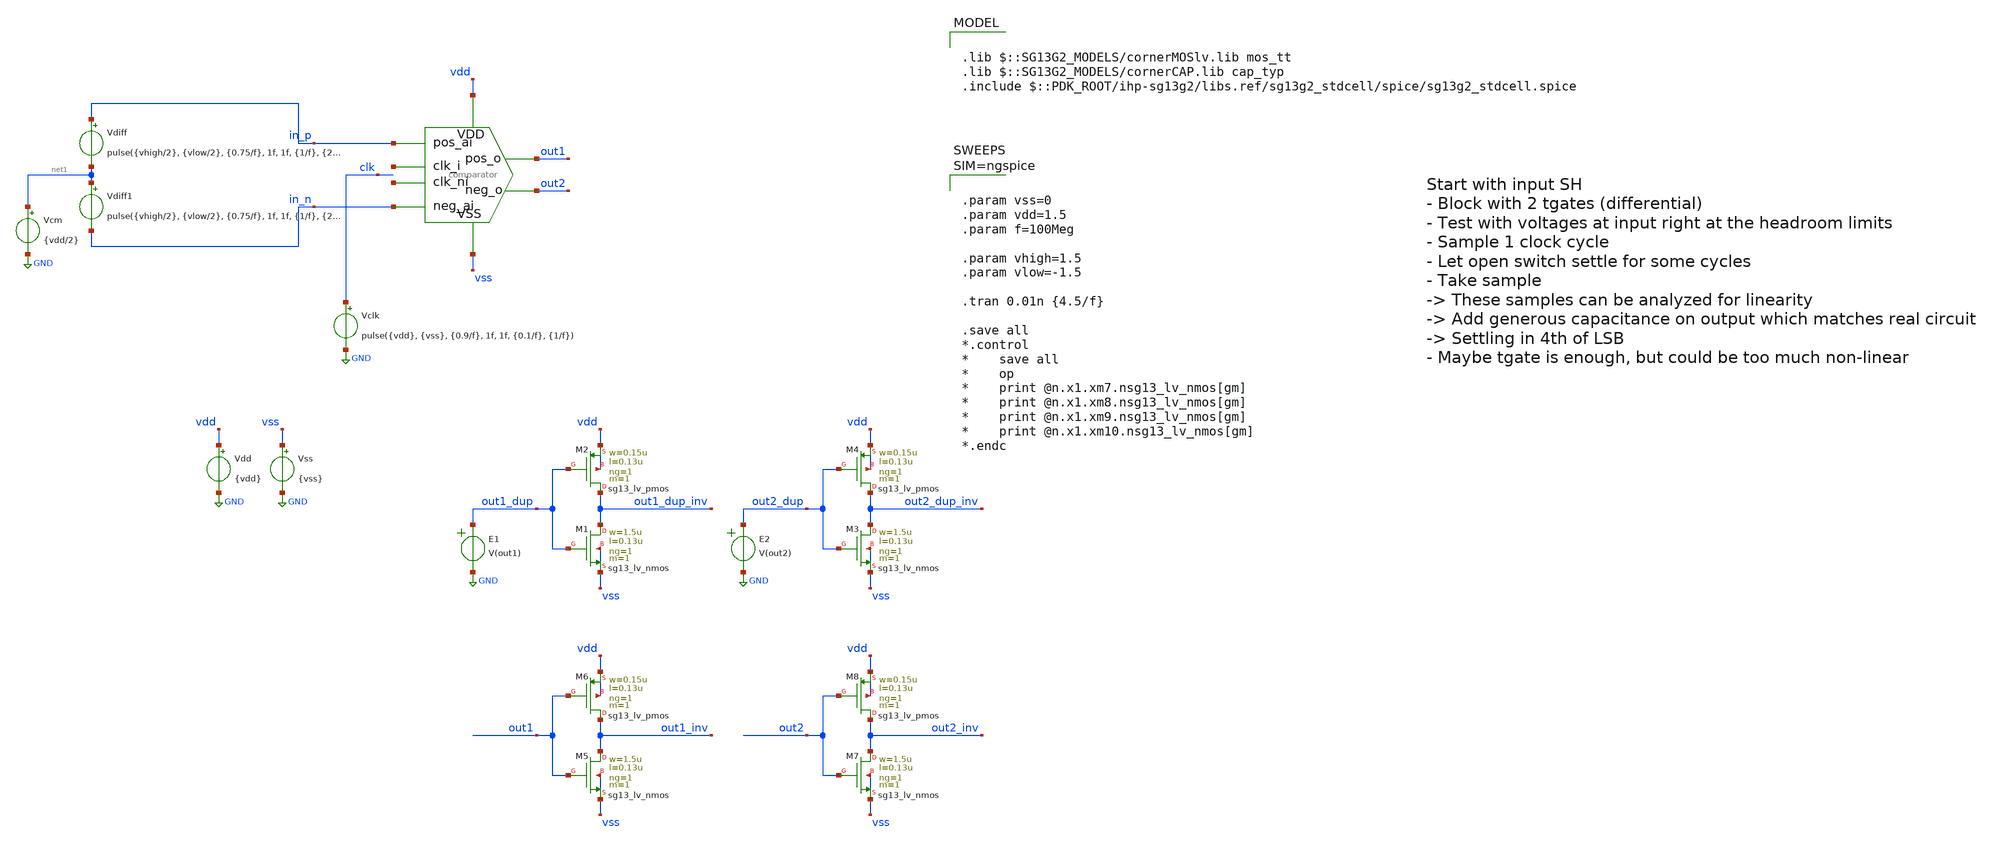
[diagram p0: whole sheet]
** sch_path: designs/comparator/comparator_tb.sch
**.subckt comparator_tb
x1 net2 in_p in_n out2 out1 vss vdd net3 comparator
Vdd vdd GND {vdd}
Vss vss GND {vss}
Vclk clk GND pulse({vdd}, {vss}, {0.9/f}, 1f, 1f, {0.1/f}, {1/f})
Vdiff in_p net1 pulse({vhigh/2}, {vlow/2}, {0.75/f}, 1f, 1f, {1/f}, {2/f})
Vcm net1 GND {vdd/2}
E1 out1_dup GND VOL=' V(out1) '
E2 out2_dup GND VOL=' V(out2) '
XM5 out1_inv out1 vss vss sg13_lv_nmos w=1.5u l=0.13u ng=1 m=1 mm_ok=1
XM6 out1_inv out1 vdd vdd sg13_lv_pmos w=0.15u l=0.13u ng=1 m=1 mm_ok=1
XM7 out2_inv out2 vss vss sg13_lv_nmos w=1.5u l=0.13u ng=1 m=1 mm_ok=1
XM8 out2_inv out2 vdd vdd sg13_lv_pmos w=0.15u l=0.13u ng=1 m=1 mm_ok=1
XM1 out1_dup_inv out1_dup vss vss sg13_lv_nmos w=1.5u l=0.13u ng=1 m=1 mm_ok=1
XM2 out1_dup_inv out1_dup vdd vdd sg13_lv_pmos w=0.15u l=0.13u ng=1 m=1 mm_ok=1
XM3 out2_dup_inv out2_dup vss vss sg13_lv_nmos w=1.5u l=0.13u ng=1 m=1 mm_ok=1
XM4 out2_dup_inv out2_dup vdd vdd sg13_lv_pmos w=0.15u l=0.13u ng=1 m=1 mm_ok=1
Vdiff1 net1 in_n pulse({vhigh/2}, {vlow/2}, {0.75/f}, 1f, 1f, {1/f}, {2/f})
**** begin user architecture code

.lib $::SG13G2_MODELS/cornerMOSlv.lib mos_tt
.lib $::SG13G2_MODELS/cornerCAP.lib cap_typ
.include $::PDK_ROOT/ihp-sg13g2/libs.ref/sg13g2_stdcell/spice/sg13g2_stdcell.spice




.param vss=0
.param vdd=1.5
.param f=100Meg

.param vhigh=1.5
.param vlow=-1.5

.tran 0.01n {4.5/f}

.save all
*.control
*	save all
*	op
*	print @n.x1.xm7.nsg13_lv_nmos[gm]
*	print @n.x1.xm8.nsg13_lv_nmos[gm]
*	print @n.x1.xm9.nsg13_lv_nmos[gm]
*	print @n.x1.xm10.nsg13_lv_nmos[gm]
*.endc



**** end user architecture code
**.ends

* expanding   symbol:  comparator.sym # of pins=8
** sym_path: designs/comparator_dt/comparator.sym
** sch_path: designs/comparator_dt/comparator.sch
.subckt comparator clk_i pos_ai neg_ai neg_o pos_o VSS VDD clk_ni
*.ipin pos_ai
*.ipin neg_ai
*.ipin VSS
*.ipin VDD
*.opin neg_o
*.opin pos_o
*.ipin clk_i
*.ipin clk_ni
XM12 neg_buf clk_i VDD VDD sg13_lv_pmos w=1.0u l=0.13u ng=1 m=1 mm_ok=1
XM13 pos_buf clk_i VDD VDD sg13_lv_pmos w=1.0u l=0.13u ng=1 m=1 mm_ok=1
XM14 net1 pos_ai neg_buf VSS sg13_lv_nmos w=1.0u l=0.13u ng=1 m=1 mm_ok=1
XM15 net1 neg_ai pos_buf VSS sg13_lv_nmos w=1.0u l=0.13u ng=1 m=1 mm_ok=1
XM16 VSS clk_i net1 VSS sg13_lv_nmos w=1.0u l=0.13u ng=1 m=1 mm_ok=1
XM17 net2 clk_ni VDD VDD sg13_lv_pmos w=2.0u l=0.13u ng=2 m=1 mm_ok=1
XM18 pos_o neg_o net2 VDD sg13_lv_pmos w=2.0u l=0.13u ng=2 m=1 mm_ok=1
XM19 neg_o pos_o net2 VDD sg13_lv_pmos w=2.0u l=0.13u ng=2 m=1 mm_ok=1
XM20 VSS neg_buf pos_o VSS sg13_lv_nmos w=1.0u l=0.13u ng=1 m=1 mm_ok=1
XM21 VSS neg_o pos_o VSS sg13_lv_nmos w=1.0u l=0.13u ng=1 m=1 mm_ok=1
XM22 VSS pos_o neg_o VSS sg13_lv_nmos w=1.0u l=0.13u ng=1 m=1 mm_ok=1
XM23 VSS pos_buf neg_o VSS sg13_lv_nmos w=1.0u l=0.13u ng=1 m=1 mm_ok=1
XC1 neg_buf VSS cap_cmim w=1.41e-5 l=1.41e-5 m=1 mm_ok=1
XC2 pos_buf VSS cap_cmim w=1.41e-5 l=1.41e-5 m=1 mm_ok=1
.ends

.GLOBAL GND
.end
